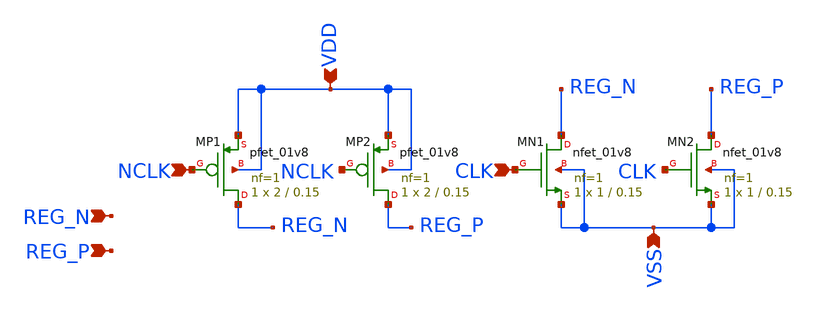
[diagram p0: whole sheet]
** sch_path: strongarm_precharge.sch
**.subckt strongarm_precharge CLK NCLK REG_N REG_P VDD VSS
*.ipin CLK
*.ipin NCLK
*.ipin REG_N
*.ipin REG_P
*.ipin VDD
*.ipin VSS
XMP1 REG_N NCLK VDD VDD sky130_fd_pr__pfet_01v8 L=0.15 W=2 nf=1 ad='int((1 + 1)/2) * 2 / 1 * 0.29' as='int((1 + 2)/2) * 2 / 1 * 0.29'
+ pd='2*int((1 + 1)/2) * (2 / 1 + 0.29)' ps='2*int((1 + 2)/2) * (2 / 1 + 0.29)' nrd='0.29 / 2 ' nrs='0.29 / 2 '
+ sa=0 sb=0 sd=0 mult=1 m=1
XMP2 REG_P NCLK VDD VDD sky130_fd_pr__pfet_01v8 L=0.15 W=2 nf=1 ad='int((1 + 1)/2) * 2 / 1 * 0.29' as='int((1 + 2)/2) * 2 / 1 * 0.29'
+ pd='2*int((1 + 1)/2) * (2 / 1 + 0.29)' ps='2*int((1 + 2)/2) * (2 / 1 + 0.29)' nrd='0.29 / 2 ' nrs='0.29 / 2 '
+ sa=0 sb=0 sd=0 mult=1 m=1
XMN1 REG_N CLK VSS VSS sky130_fd_pr__nfet_01v8 L=0.15 W=1 nf=1 ad='int((1 + 1)/2) * 1 / 1 * 0.29' as='int((1 + 2)/2) * 1 / 1 * 0.29'
+ pd='2*int((1 + 1)/2) * (1 / 1 + 0.29)' ps='2*int((1 + 2)/2) * (1 / 1 + 0.29)' nrd='0.29 / 1 ' nrs='0.29 / 1 '
+ sa=0 sb=0 sd=0 mult=1 m=1
XMN2 REG_P CLK VSS VSS sky130_fd_pr__nfet_01v8 L=0.15 W=1 nf=1 ad='int((1 + 1)/2) * 1 / 1 * 0.29' as='int((1 + 2)/2) * 1 / 1 * 0.29'
+ pd='2*int((1 + 1)/2) * (1 / 1 + 0.29)' ps='2*int((1 + 2)/2) * (1 / 1 + 0.29)' nrd='0.29 / 1 ' nrs='0.29 / 1 '
+ sa=0 sb=0 sd=0 mult=1 m=1
**.ends
.end
